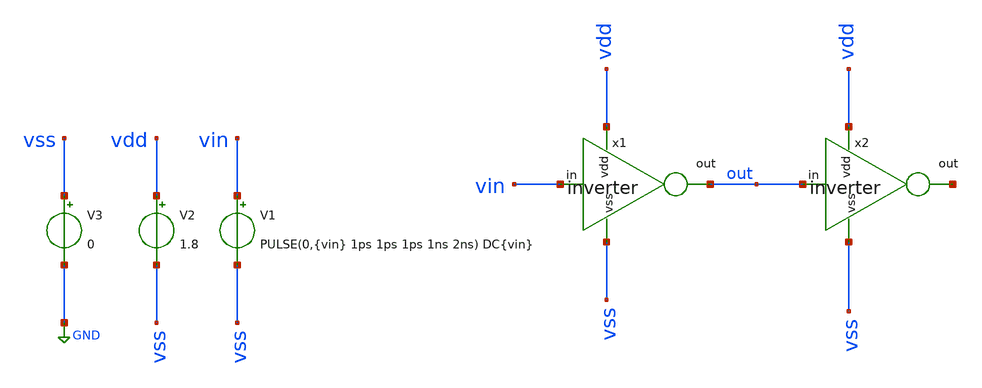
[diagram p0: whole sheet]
** sch_path: src/inverter/tb_inverter.sch
**.subckt tb_inverter
x1 vdd out vin vss inverter
V1 vin vss PULSE(0,{vin} 1ps 1ps 1ps 1ns 2ns) DC{vin}
V2 vdd vss 1.8
V3 vss GND 0
x2 vdd net1 out vss inverter
**** begin user architecture code



*Parametros del circuito
.param vin=1.8
.options TEMP = 27.0 *deafult

*Include
.lib /home/eamta/skywater/skywater-pdk/libraries/sky130_fd_pr_ngspice/latest/models/corners/sky130.lib TT

*Signal to Save
.save all   @M.x1.xM1.msky130_fd_pr__nfet_01v8[id] @M.x1.xM1.msky130_fd_pr__nfet_01v8[gm]  @M.x1.xM2.msky130_fd_pr__pfet_01v8[id] @M.x1.xM2.msky130_fd_pr__pfet_01v8[gm]

*Simulacion
.control
* let start_WN =0.45
* let stop_WN  =2
* let delta_WN =0.45
* let init_WN  = star_WN
 *loop
* setplot dc
* while init_WN le stop_WN
*  alter Wn init_WN
*  run
*  *write dc-sweep.out v(out)
*  set appendwrite
*  dc v1 0 1.8 0.01
  *setplot dc1
*  plot v(out) v(vin)

 tran 0.01n 10ns
 setplot tran1
 plot v(out) v(vin)
 set filetype = ascii *para guardar en ascii
 write tb_inverter_tran.raw

 reset

 dc v1 0 1.8 0.01
 setplot dc1
 plot v(out) v(vin)
 set filetype = ascii
 write tb_inverter_dc.raw

 reset

 op
 set filetype = ascii
 write tb_inverter.raw
 print all

 reset
 dc v1 0 1.8 0.01
 setplot id
 plot @M.x1.xM1.msky130_fd_pr__nfet_01v8[id]
 set filetype = ascii
 write tb_inverter_id.raw

.endc


.end


**** end user architecture code
**.ends

* expanding   symbol:  inverter/inverter.sym # of pins=4
** sym_path: src/inverter/inverter.sym
** sch_path: src/inverter/inverter.sch
.subckt inverter vdd out in vss
*.opin out
*.ipin in
*.ipin vss
*.ipin vdd
XM1 out in vss vss sky130_fd_pr__nfet_01v8 L=0.15 W=0.45 nf=1 ad='int((nf+1)/2) * W/nf * 0.29' as='int((nf+2)/2) * W/nf * 0.29'
+ pd='2*int((nf+1)/2) * (W/nf + 0.29)' ps='2*int((nf+2)/2) * (W/nf + 0.29)' nrd='0.29 / W' nrs='0.29 / W'
+ sa=0 sb=0 sd=0 mult=1 m=1
XM2 out in vdd vdd sky130_fd_pr__pfet_01v8 L=0.15 W=0.9 nf=1 ad='int((nf+1)/2) * W/nf * 0.29' as='int((nf+2)/2) * W/nf * 0.29'
+ pd='2*int((nf+1)/2) * (W/nf + 0.29)' ps='2*int((nf+2)/2) * (W/nf + 0.29)' nrd='0.29 / W' nrs='0.29 / W'
+ sa=0 sb=0 sd=0 mult=1 m=1
.ends

.GLOBAL GND
.end
